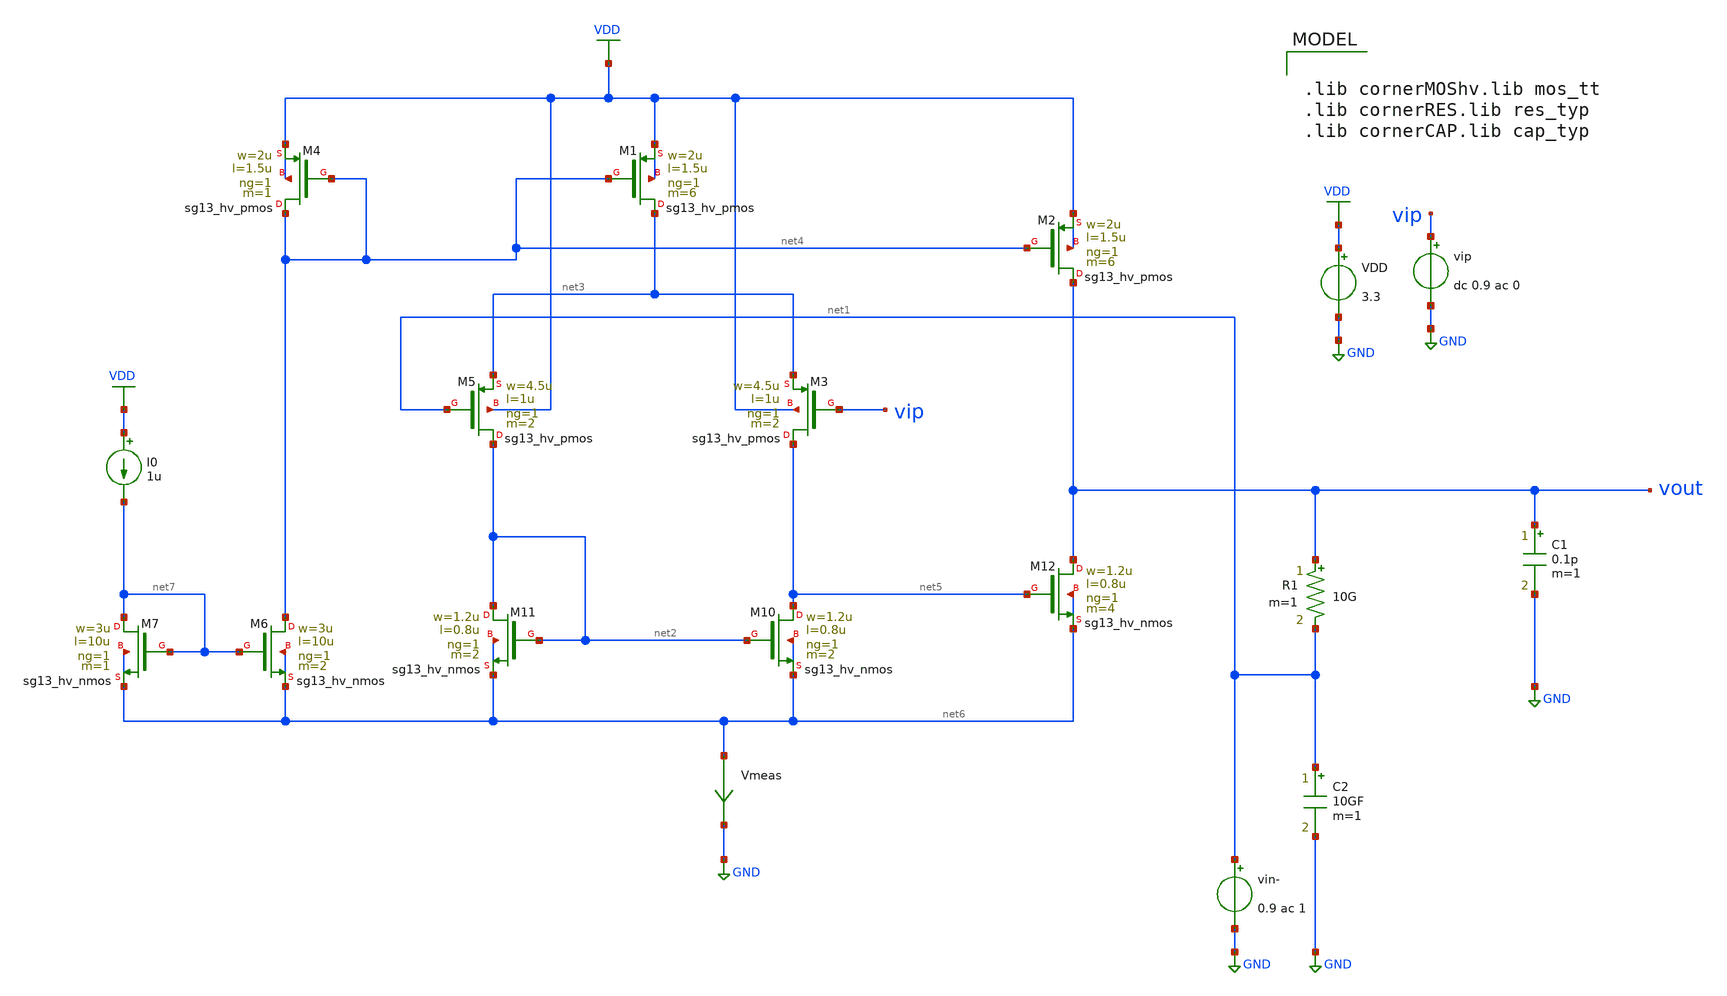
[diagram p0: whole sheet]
** sch_path: dependencies/ClockExtractor/ClockExtractor-main/schematic/xschem/schematic/TowStageOTA_AC_2026.sch
**.subckt TowStageOTA_AC_2026
vip vip GND dc 0.9 ac 0
C2 net1 GND 10GF m=1
R1 vout net1 10G m=1
vin- net1 GND 0.9 ac 1
C1 vout GND 0.1p m=1
VDD VDD GND 3.3
XM4 net4 net4 VDD VDD sg13_hv_pmos w=2u l=1.5u ng=1 m=1 mm_ok=1
XM1 net3 net4 VDD VDD sg13_hv_pmos w=2u l=1.5u ng=1 m=6 mm_ok=1
XM2 vout net4 VDD VDD sg13_hv_pmos w=2u l=1.5u ng=1 m=6 mm_ok=1
XM3 net5 vip net3 VDD sg13_hv_pmos w=4.5u l=1u ng=1 m=2 mm_ok=1
XM5 net2 net1 net3 VDD sg13_hv_pmos w=4.5u l=1u ng=1 m=2 mm_ok=1
XM10 net5 net2 net6 net6 sg13_hv_nmos w=1.2u l=0.8u ng=1 m=2 mm_ok=1
XM11 net2 net2 net6 net6 sg13_hv_nmos w=1.2u l=0.8u ng=1 m=2 mm_ok=1
XM12 vout net5 net6 net6 sg13_hv_nmos w=1.2u l=0.8u ng=1 m=4 mm_ok=1
I0 VDD net7 1u
Vmeas net6 GND 0
.save i(vmeas)
XM6 net4 net7 net6 net6 sg13_hv_nmos w=3u l=10u ng=1 m=2 mm_ok=1
XM7 net7 net7 net6 net6 sg13_hv_nmos w=3u l=10u ng=1 m=1 mm_ok=1
**** begin user architecture code

.lib cornerMOShv.lib mos_tt
.lib cornerRES.lib res_typ
.lib cornerCAP.lib cap_typ



.param temp=27
.control
save all
op
ac dec 100 1 2G
let gain_db = db(v(vout))
let phase = ph(v(vout))*180/pi
meas ac dc_gain find vdb(vout) at=1
 meas ac gain_at_13_56MHz find vdb(vout) at=13.56meg
  let 3dB_gain = dc_gain - 3
  meas ac bandwidth when vdb(vout)=3dB_gain fall=1
 print dc_gain
 print 3dB_gain
 print bandwidth

 meas ac unity_freq when gain_db=0
 meas ac phase_at_unity find phase at=unity_freq
 let phase_margin = 180 - phase_at_unity

 print unity_freq
 print phase_margin

 print gain_at_13_56MHz


 plot db(v(vout))
 plot cph(v(vout))*180/pi

write TowStageOTA_AC_2026.raw
.endc


**** end user architecture code
**.ends
.GLOBAL GND
.GLOBAL VDD
.end
